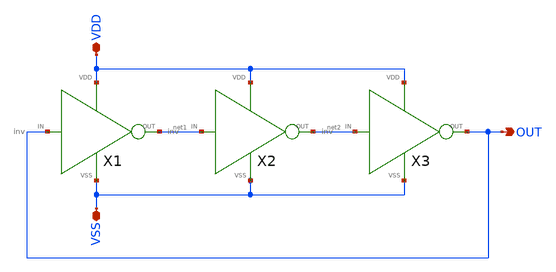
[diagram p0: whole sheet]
** sch_path: ringosc/ringosc.sch
**.subckt ringosc VDD VSS OUT
*.iopin VDD
*.iopin VSS
*.opin OUT
X1 OUT net1 VSS VDD inv
X2 net1 net2 VSS VDD inv
X3 net2 OUT VSS VDD inv
**.ends

* expanding   symbol:  /home/brito/sky130_opensource_skel/opencryo/ringosc/inv.sym # of pins=4
** sym_path: ringosc/inv.sym
** sch_path: ringosc/inv.sch
.subckt inv IN OUT VSS VDD
*.ipin IN
*.iopin VSS
*.opin OUT
*.iopin VDD
XM1 OUT IN VSS VSS sky130_fd_pr__nfet_01v8 L=0.15 W=1 nf=1 ad='int((nf+1)/2) * W/nf * 0.29' as='int((nf+2)/2) * W/nf * 0.29'
+ pd='2*int((nf+1)/2) * (W/nf + 0.29)' ps='2*int((nf+2)/2) * (W/nf + 0.29)' nrd='0.29 / W' nrs='0.29 / W'
+ sa=0 sb=0 sd=0 mult=1 m=1
XM2 OUT IN VDD VDD sky130_fd_pr__pfet_01v8 L=0.15 W=1 nf=1 ad='int((nf+1)/2) * W/nf * 0.29' as='int((nf+2)/2) * W/nf * 0.29'
+ pd='2*int((nf+1)/2) * (W/nf + 0.29)' ps='2*int((nf+2)/2) * (W/nf + 0.29)' nrd='0.29 / W' nrs='0.29 / W'
+ sa=0 sb=0 sd=0 mult=1 m=1
.ends

.end
